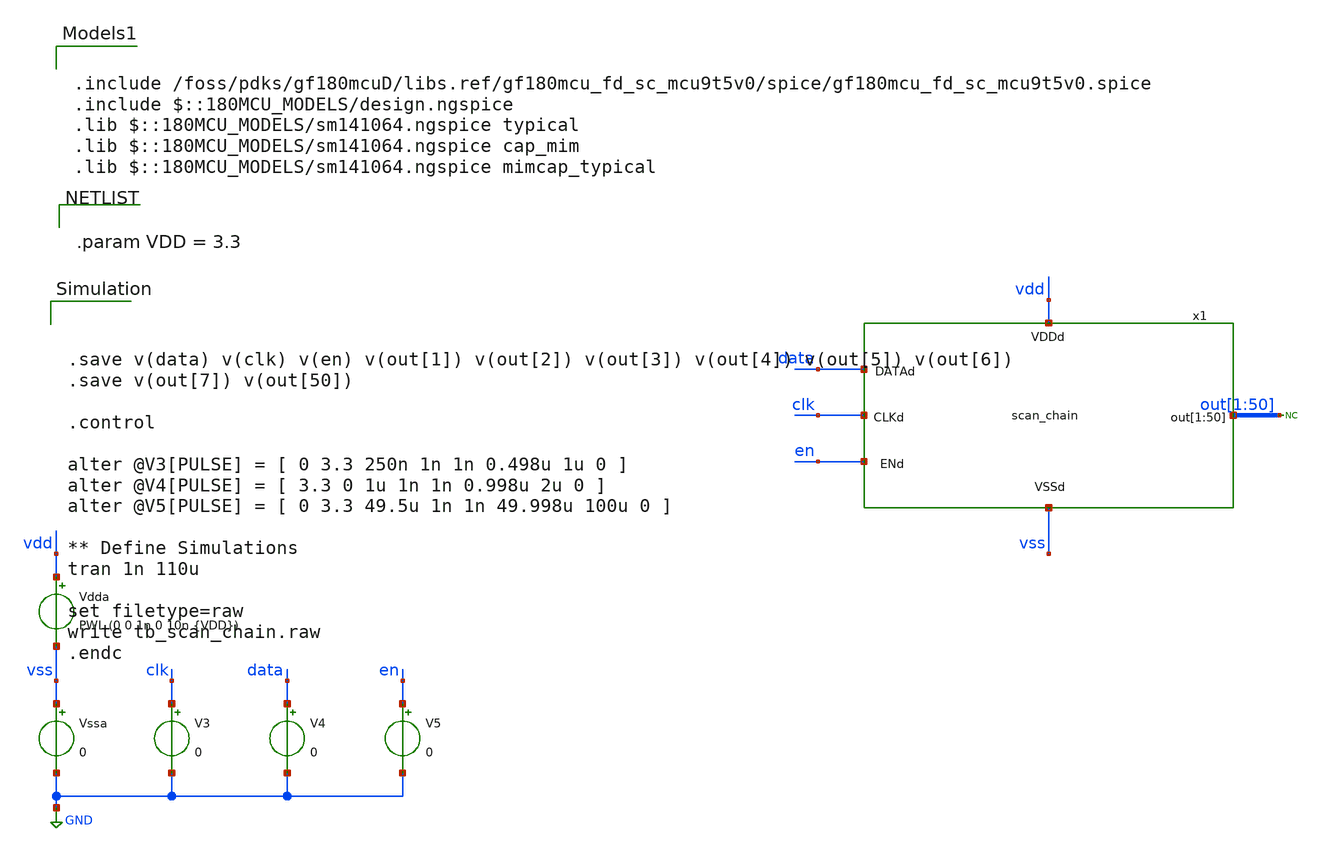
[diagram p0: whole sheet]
** sch_path: designs/libs/tb_top_level/tb_scan_chain_20250915.sch
**.subckt tb_scan_chain_20250915
Vssa vss GND 0
Vdda vdd vss PWL (0 0 1n 0 10n {VDD})
x1 vdd vss clk en data out[1] out[2] out[3] out[4] out[5] out[6] out[7] out[8] out[9] out[10]
+ out[11] out[12] out[13] out[14] out[15] out[16] out[17] out[18] out[19] out[20] out[21] out[22] out[23]
+ out[24] out[25] out[26] out[27] out[28] out[29] out[30] out[31] out[32] out[33] out[34] out[35] out[36]
+ out[37] out[38] out[39] out[40] out[41] out[42] out[43] out[44] out[45] out[46] out[47] out[48] out[49]
+ out[50] scan_chain
* noconn out[1:50]
V3 clk GND 0
V4 data GND 0
V5 en GND 0
**** begin user architecture code

.include /foss/pdks/gf180mcuD/libs.ref/gf180mcu_fd_sc_mcu9t5v0/spice/gf180mcu_fd_sc_mcu9t5v0.spice
.include $::180MCU_MODELS/design.ngspice
.lib $::180MCU_MODELS/sm141064.ngspice typical
.lib $::180MCU_MODELS/sm141064.ngspice cap_mim
.lib $::180MCU_MODELS/sm141064.ngspice mimcap_typical



.param VDD = 3.3





.save v(data) v(clk) v(en) v(out[1]) v(out[2]) v(out[3]) v(out[4]) v(out[5]) v(out[6])
.save v(out[7]) v(out[50])

.control

alter @V3[PULSE] = [ 0 3.3 250n 1n 1n 0.498u 1u 0 ]
alter @V4[PULSE] = [ 3.3 0 1u 1n 1n 0.998u 2u 0 ]
alter @V5[PULSE] = [ 0 3.3 49.5u 1n 1n 49.998u 100u 0 ]

** Define Simulations
tran 1n 110u

set filetype=raw
write tb_scan_chain.raw
.endc


**** end user architecture code
**.ends
.GLOBAL GND
.end
